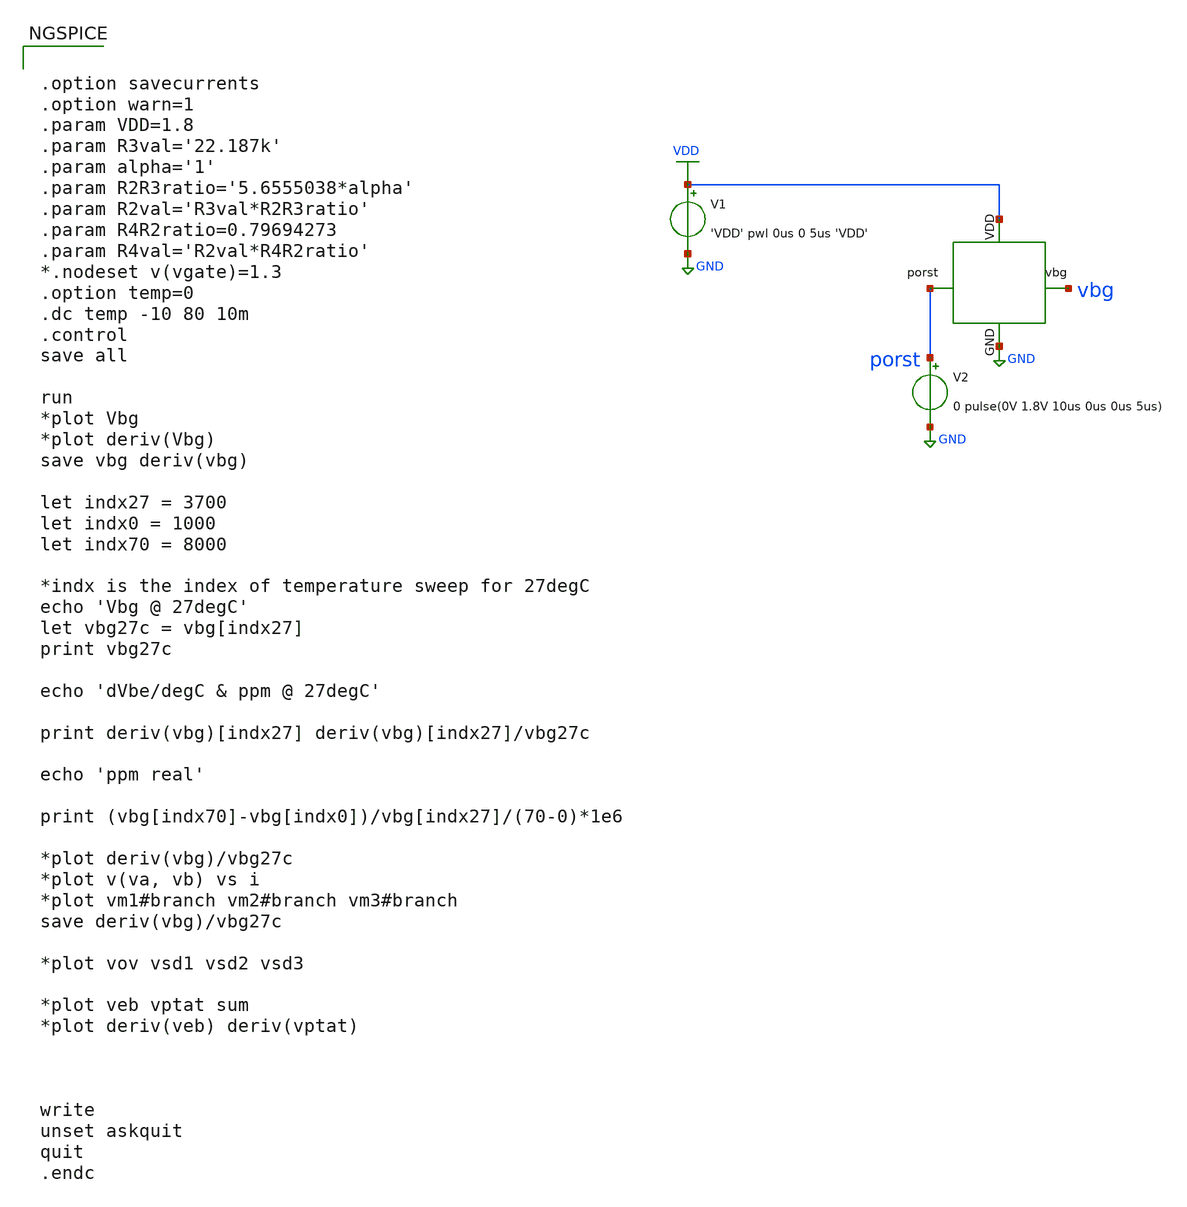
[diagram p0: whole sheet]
** sch_path: tests/tempsweep/tsmc_bandgap_real_tempsweep.sch
**.subckt tsmc_bandgap_real_tempsweep
V1 VDD GND 'VDD' pwl 0us 0 5us 'VDD'
V2 porst GND 0 pulse(0V 1.8V 10us 0us 0us 5us)
**** begin user architecture code


.option savecurrents
.option warn=1
.param VDD=1.8
.param R3val='22.187k'
.param alpha='1'
.param R2R3ratio='5.6555038*alpha'
.param R2val='R3val*R2R3ratio'
.param R4R2ratio=0.79694273
.param R4val='R2val*R4R2ratio'
*.nodeset v(vgate)=1.3
.option temp=0
.dc temp -10 80 10m
.control
save all

run
*plot Vbg
*plot deriv(Vbg)
save vbg deriv(vbg)

let indx27 = 3700
let indx0 = 1000
let indx70 = 8000

*indx is the index of temperature sweep for 27degC
echo 'Vbg @ 27degC'
let vbg27c = vbg[indx27]
print vbg27c

echo 'dVbe/degC & ppm @ 27degC'

print deriv(vbg)[indx27] deriv(vbg)[indx27]/vbg27c

echo 'ppm real'

print (vbg[indx70]-vbg[indx0])/vbg[indx27]/(70-0)*1e6

*plot deriv(vbg)/vbg27c
*plot v(va, vb) vs i
*plot vm1#branch vm2#branch vm3#branch
save deriv(vbg)/vbg27c

*plot vov vsd1 vsd2 vsd3

*plot veb vptat sum
*plot deriv(veb) deriv(vptat)



write
unset askquit
quit
.endc



** opencircuitdesign pdks install
.lib $::SKYWATER_MODELS/sky130.lib.spice tt


**** end user architecture code
**.ends
.GLOBAL VDD
.GLOBAL GND
.end
